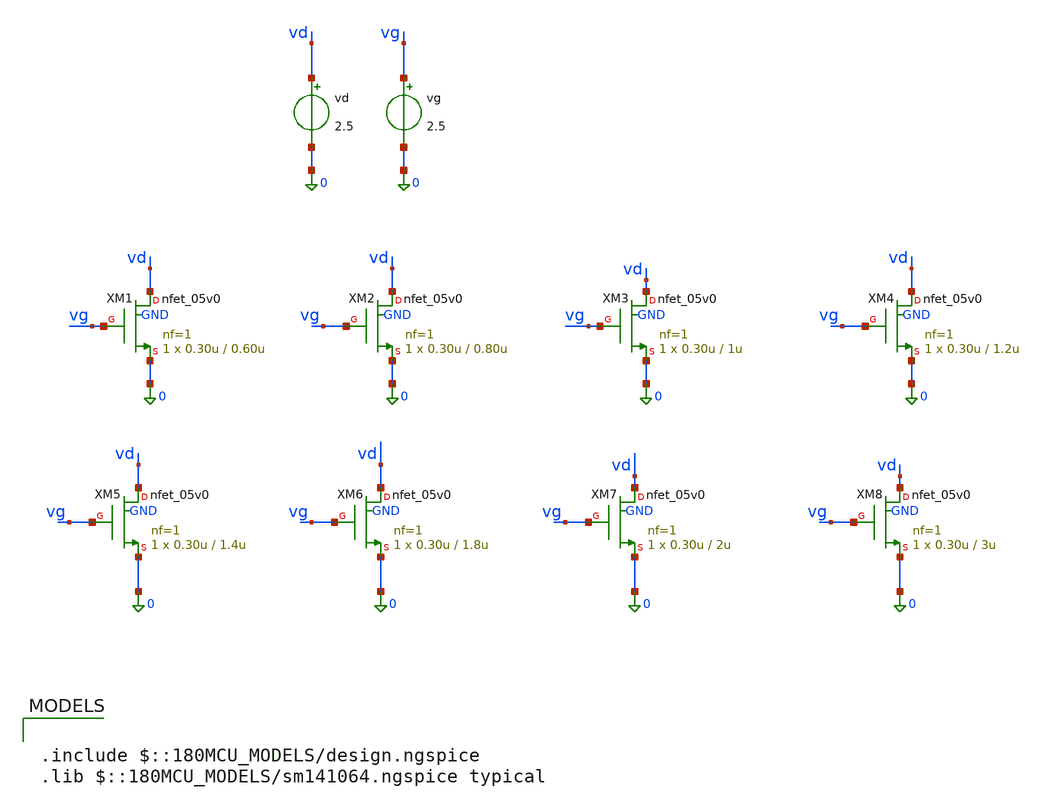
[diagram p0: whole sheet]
** sch_path: Gm_ID Design Charts (GF 180 MCU) For BGR/Schematic/gmid_gf180_nmos.sch
**.subckt gmid_gf180_nmos
XM1 vd vg 0 GND nfet_05v0 L=0.60u W=0.30u nf=1 ad='int((nf+1)/2) * W/nf * 0.18u' as='int((nf+2)/2) * W/nf * 0.18u'
+ pd='2*int((nf+1)/2) * (W/nf + 0.18u)' ps='2*int((nf+2)/2) * (W/nf + 0.18u)' nrd='0.18u / W' nrs='0.18u / W'
+ sa=0 sb=0 sd=0 m=1 par=1
XM2 vd vg 0 GND nfet_05v0 L=0.80u W=0.30u nf=1 ad='int((nf+1)/2) * W/nf * 0.18u' as='int((nf+2)/2) * W/nf * 0.18u'
+ pd='2*int((nf+1)/2) * (W/nf + 0.18u)' ps='2*int((nf+2)/2) * (W/nf + 0.18u)' nrd='0.18u / W' nrs='0.18u / W'
+ sa=0 sb=0 sd=0 m=1 par=1
XM3 vd vg 0 GND nfet_05v0 L=1u W=0.30u nf=1 ad='int((nf+1)/2) * W/nf * 0.18u' as='int((nf+2)/2) * W/nf * 0.18u'
+ pd='2*int((nf+1)/2) * (W/nf + 0.18u)' ps='2*int((nf+2)/2) * (W/nf + 0.18u)' nrd='0.18u / W' nrs='0.18u / W'
+ sa=0 sb=0 sd=0 m=1 par=1
XM4 vd vg 0 GND nfet_05v0 L=1.2u W=0.30u nf=1 ad='int((nf+1)/2) * W/nf * 0.18u' as='int((nf+2)/2) * W/nf * 0.18u'
+ pd='2*int((nf+1)/2) * (W/nf + 0.18u)' ps='2*int((nf+2)/2) * (W/nf + 0.18u)' nrd='0.18u / W' nrs='0.18u / W'
+ sa=0 sb=0 sd=0 m=1 par=1
XM5 vd vg 0 GND nfet_05v0 L=1.4u W=0.30u nf=1 ad='int((nf+1)/2) * W/nf * 0.18u' as='int((nf+2)/2) * W/nf * 0.18u'
+ pd='2*int((nf+1)/2) * (W/nf + 0.18u)' ps='2*int((nf+2)/2) * (W/nf + 0.18u)' nrd='0.18u / W' nrs='0.18u / W'
+ sa=0 sb=0 sd=0 m=1 par=1
XM6 vd vg 0 GND nfet_05v0 L=1.8u W=0.30u nf=1 ad='int((nf+1)/2) * W/nf * 0.18u' as='int((nf+2)/2) * W/nf * 0.18u'
+ pd='2*int((nf+1)/2) * (W/nf + 0.18u)' ps='2*int((nf+2)/2) * (W/nf + 0.18u)' nrd='0.18u / W' nrs='0.18u / W'
+ sa=0 sb=0 sd=0 m=1 par=1
XM7 vd vg 0 GND nfet_05v0 L=2u W=0.30u nf=1 ad='int((nf+1)/2) * W/nf * 0.18u' as='int((nf+2)/2) * W/nf * 0.18u'
+ pd='2*int((nf+1)/2) * (W/nf + 0.18u)' ps='2*int((nf+2)/2) * (W/nf + 0.18u)' nrd='0.18u / W' nrs='0.18u / W'
+ sa=0 sb=0 sd=0 m=1 par=1
XM8 vd vg 0 GND nfet_05v0 L=3u W=0.30u nf=1 ad='int((nf+1)/2) * W/nf * 0.18u' as='int((nf+2)/2) * W/nf * 0.18u'
+ pd='2*int((nf+1)/2) * (W/nf + 0.18u)' ps='2*int((nf+2)/2) * (W/nf + 0.18u)' nrd='0.18u / W' nrs='0.18u / W'
+ sa=0 sb=0 sd=0 m=1 par=1
vd vd 0 2.5
vg vg 0 2.5
**** begin user architecture code

.include $::180MCU_MODELS/design.ngspice
.lib $::180MCU_MODELS/sm141064.ngspice typical



.option wnflag=1
.option savecurrents
.control

save @m.xm1.m0[gm]
save @m.xm1.m0[vth]
save @m.xm1.m0[gds]
save @m.xm1.m0[id]
save @m.xm1.m0[vds]
save @m.xm1.m0[cgg]
save @m.xm1.m0[vgs]

save @m.xm2.m0[gm]
save @m.xm2.m0[vth]
save @m.xm2.m0[gds]
save @m.xm2.m0[id]
save @m.xm2.m0[vds]
save @m.xm2.m0[cgg]
save @m.xm2.m0[vgs]

save @m.xm3.m0[gm]
save @m.xm3.m0[vth]
save @m.xm3.m0[gds]
save @m.xm3.m0[id]
save @m.xm3.m0[vds]
save @m.xm3.m0[cgg]
save @m.xm3.m0[vgs]

save @m.xm4.m0[gm]
save @m.xm4.m0[vth]
save @m.xm4.m0[gds]
save @m.xm4.m0[id]
save @m.xm4.m0[vds]
save @m.xm4.m0[cgg]
save @m.xm4.m0[vgs]

save @m.xm5.m0[gm]
save @m.xm5.m0[vth]
save @m.xm5.m0[gds]
save @m.xm5.m0[id]
save @m.xm5.m0[vds]
save @m.xm5.m0[cgg]
save @m.xm5.m0[vgs]

save @m.xm6.m0[gm]
save @m.xm6.m0[vth]
save @m.xm6.m0[gds]
save @m.xm6.m0[id]
save @m.xm6.m0[vds]
save @m.xm6.m0[cgg]
save @m.xm6.m0[vgs]

save @m.xm7.m0[gm]
save @m.xm7.m0[vth]
save @m.xm7.m0[gds]
save @m.xm7.m0[id]
save @m.xm7.m0[vds]
save @m.xm7.m0[cgg]
save @m.xm7.m0[vgs]

save @m.xm8.m0[gm]
save @m.xm8.m0[vth]
save @m.xm8.m0[gds]
save @m.xm8.m0[id]
save @m.xm8.m0[vds]
save @m.xm8.m0[cgg]
save @m.xm8.m0[vgs]

dc VG 0.05 5 0.01
remzerovec

write gf180_nmos_5V.raw

wrdata gmid_gf180_nmos51.txt  @m.xm1.m0[gm]  @m.xm1.m0[gds]  @m.xm1.m0[id]  @m.xm1.m0[w]
+  @m.xm1.m0[vds]  @m.xm1.m0[cgg]  @m.xm1.m0[vgs]  @m.xm1.m0[vth]

wrdata gmid_gf180_nmos52.txt  @m.xm2.m0[gm]  @m.xm2.m0[gds]  @m.xm2.m0[id]  @m.xm2.m0[w]
+  @m.xm2.m0[vds]  @m.xm2.m0[cgg]  @m.xm2.m0[vgs]  @m.xm2.m0[vth]

wrdata gmid_gf180_nmos53.txt  @m.xm3.m0[gm]  @m.xm3.m0[gds]  @m.xm3.m0[id]  @m.xm3.m0[w]
+  @m.xm3.m0[vds]  @m.xm3.m0[cgg]  @m.xm3.m0[vgs]  @m.xm3.m0[vth]

wrdata gmid_gf180_nmos54.txt  @m.xm4.m0[gm]  @m.xm4.m0[gds]  @m.xm4.m0[id]  @m.xm4.m0[w]
+  @m.xm4.m0[vds]  @m.xm4.m0[cgg]  @m.xm4.m0[vgs]  @m.xm4.m0[vth]

wrdata gmid_gf180_nmos55.txt  @m.xm5.m0[gm]  @m.xm5.m0[gds]  @m.xm5.m0[id]  @m.xm5.m0[w]
+  @m.xm5.m0[vds]  @m.xm5.m0[cgg]  @m.xm5.m0[vgs]  @m.xm5.m0[vth]

wrdata gmid_gf180_nmos56.txt  @m.xm6.m0[gm]  @m.xm6.m0[gds]  @m.xm6.m0[id]  @m.xm6.m0[w]
+  @m.xm6.m0[vds]  @m.xm6.m0[cgg]  @m.xm6.m0[vgs]  @m.xm6.m0[vth]

wrdata gmid_gf180_nmos57.txt  @m.xm7.m0[gm]  @m.xm7.m0[gds]  @m.xm7.m0[id]  @m.xm7.m0[w]
+  @m.xm7.m0[vds]  @m.xm7.m0[cgg]  @m.xm7.m0[vgs]  @m.xm7.m0[vth]

wrdata gmid_gf180_nmos58.txt  @m.xm8.m0[gm]  @m.xm8.m0[gds]  @m.xm8.m0[id]  @m.xm8.m0[w]
+  @m.xm8.m0[vds]  @m.xm8.m0[cgg]  @m.xm8.m0[vgs]  @m.xm8.m0[vth]

set appendwrite
remzerovec
.endc


**** end user architecture code
**.ends
.end
